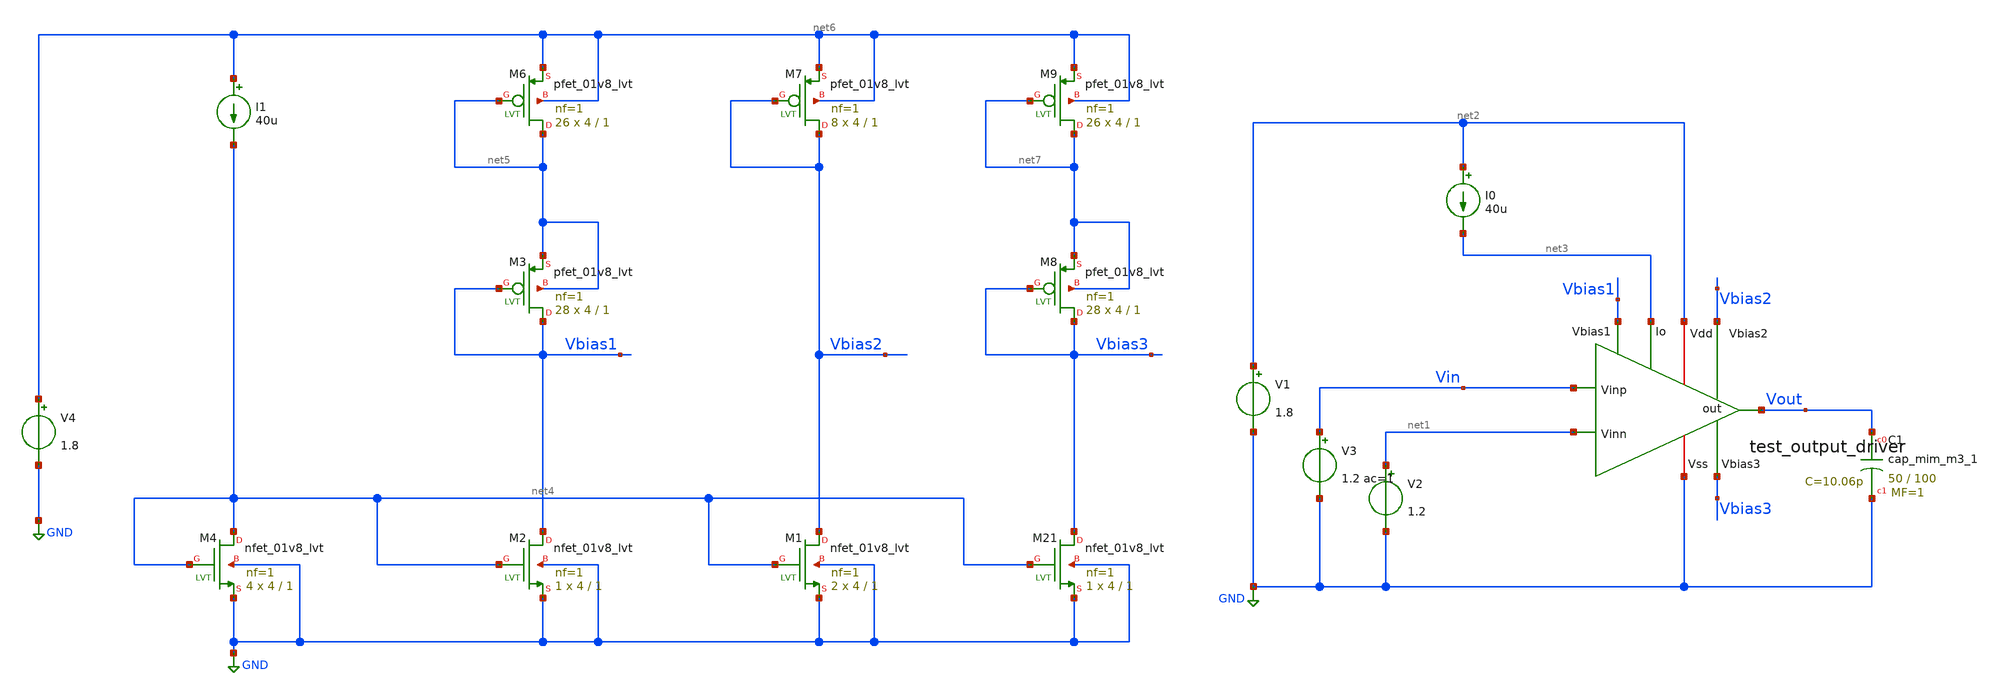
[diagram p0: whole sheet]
** sch_path: xschem/ip_block/opamp/folded_cas_xiaoyi/tb_test_output_driver.sch
**.subckt tb_test_output_driver
V1 net2 GND 1.8
V2 net1 GND 1.2
V3 Vin GND 1.2 ac=1
I0 net2 net3 40u
XC1 Vout GND sky130_fd_pr__cap_mim_m3_1 W=50 L=100 MF=1 m=1
x1 net2 net1 Vin Vout net3 GND Vbias1 Vbias2 Vbias3 test_output_driver
XM2 Vbias1 net4 GND GND sky130_fd_pr__nfet_01v8_lvt L=1 W=4 nf=1 ad='int((nf+1)/2) * W/nf * 0.29' as='int((nf+2)/2) * W/nf * 0.29'
+ pd='2*int((nf+1)/2) * (W/nf + 0.29)' ps='2*int((nf+2)/2) * (W/nf + 0.29)' nrd='0.29 / W' nrs='0.29 / W'
+ sa=0 sb=0 sd=0 mult=1 m=1
XM3 Vbias1 Vbias1 net5 net5 sky130_fd_pr__pfet_01v8_lvt L=1 W=4 nf=1 ad='int((nf+1)/2) * W/nf * 0.29'
+ as='int((nf+2)/2) * W/nf * 0.29' pd='2*int((nf+1)/2) * (W/nf + 0.29)' ps='2*int((nf+2)/2) * (W/nf + 0.29)'
+ nrd='0.29 / W' nrs='0.29 / W' sa=0 sb=0 sd=0 mult=28 m=28
I1 net6 net4 40u
XM4 net4 net4 GND GND sky130_fd_pr__nfet_01v8_lvt L=1 W=4 nf=1 ad='int((nf+1)/2) * W/nf * 0.29' as='int((nf+2)/2) * W/nf * 0.29'
+ pd='2*int((nf+1)/2) * (W/nf + 0.29)' ps='2*int((nf+2)/2) * (W/nf + 0.29)' nrd='0.29 / W' nrs='0.29 / W'
+ sa=0 sb=0 sd=0 mult=4 m=4
V4 net6 GND 1.8
XM1 Vbias2 net4 GND GND sky130_fd_pr__nfet_01v8_lvt L=1 W=4 nf=1 ad='int((nf+1)/2) * W/nf * 0.29' as='int((nf+2)/2) * W/nf * 0.29'
+ pd='2*int((nf+1)/2) * (W/nf + 0.29)' ps='2*int((nf+2)/2) * (W/nf + 0.29)' nrd='0.29 / W' nrs='0.29 / W'
+ sa=0 sb=0 sd=0 mult=2 m=2
XM21 Vbias3 net4 GND GND sky130_fd_pr__nfet_01v8_lvt L=1 W=4 nf=1 ad='int((nf+1)/2) * W/nf * 0.29' as='int((nf+2)/2) * W/nf * 0.29'
+ pd='2*int((nf+1)/2) * (W/nf + 0.29)' ps='2*int((nf+2)/2) * (W/nf + 0.29)' nrd='0.29 / W' nrs='0.29 / W'
+ sa=0 sb=0 sd=0 mult=1 m=1
XM6 net5 net5 net6 net6 sky130_fd_pr__pfet_01v8_lvt L=1 W=4 nf=1 ad='int((nf+1)/2) * W/nf * 0.29' as='int((nf+2)/2) * W/nf * 0.29'
+ pd='2*int((nf+1)/2) * (W/nf + 0.29)' ps='2*int((nf+2)/2) * (W/nf + 0.29)' nrd='0.29 / W' nrs='0.29 / W'
+ sa=0 sb=0 sd=0 mult=26 m=26
XM7 Vbias2 Vbias2 net6 net6 sky130_fd_pr__pfet_01v8_lvt L=1 W=4 nf=1 ad='int((nf+1)/2) * W/nf * 0.29'
+ as='int((nf+2)/2) * W/nf * 0.29' pd='2*int((nf+1)/2) * (W/nf + 0.29)' ps='2*int((nf+2)/2) * (W/nf + 0.29)'
+ nrd='0.29 / W' nrs='0.29 / W' sa=0 sb=0 sd=0 mult=8 m=8
XM8 Vbias3 Vbias3 net7 net7 sky130_fd_pr__pfet_01v8_lvt L=1 W=4 nf=1 ad='int((nf+1)/2) * W/nf * 0.29'
+ as='int((nf+2)/2) * W/nf * 0.29' pd='2*int((nf+1)/2) * (W/nf + 0.29)' ps='2*int((nf+2)/2) * (W/nf + 0.29)'
+ nrd='0.29 / W' nrs='0.29 / W' sa=0 sb=0 sd=0 mult=28 m=28
XM9 net7 net7 net6 net6 sky130_fd_pr__pfet_01v8_lvt L=1 W=4 nf=1 ad='int((nf+1)/2) * W/nf * 0.29' as='int((nf+2)/2) * W/nf * 0.29'
+ pd='2*int((nf+1)/2) * (W/nf + 0.29)' ps='2*int((nf+2)/2) * (W/nf + 0.29)' nrd='0.29 / W' nrs='0.29 / W'
+ sa=0 sb=0 sd=0 mult=26 m=26
**** begin user architecture code
.lib $::SKYWATER_MODELS/sky130.lib.spice tt


.option temp=27
.op
.ac dec 10 1 1G
*.tran 0.1n 100u

.control
ac dec 10 1 1G
*tran 0.1n 100u
*ac dec 10 1 1G
let phase = 180/PI*vp(Vout)

plot vdb(Vout) phase
*plot Vin_p Vout
.endc

.save all



**** end user architecture code
**.ends

* expanding   symbol:  ip_block/opamp/folded_cas_xiaoyi/test_output_driver.sym # of pins=9
** sym_path: xschem/ip_block/opamp/folded_cas_xiaoyi/test_output_driver.sym
** sch_path: xschem/ip_block/opamp/folded_cas_xiaoyi/test_output_driver.sch
.subckt test_output_driver Vdd Vinn Vinp Vout Io Vss Vbias1 Vbias2 Vbias3
*.ipin Io
*.ipin Vbias1
*.ipin Vinp
*.ipin Vinn
*.ipin Vbias2
*.ipin Vbias3
*.opin Vout
*.iopin Vdd
*.iopin Vss
XM1 net2 Vinp net1 Vss sky130_fd_pr__nfet_01v8_lvt L=1 W=8 nf=1 ad='int((nf+1)/2) * W/nf * 0.29' as='int((nf+2)/2) * W/nf * 0.29'
+ pd='2*int((nf+1)/2) * (W/nf + 0.29)' ps='2*int((nf+2)/2) * (W/nf + 0.29)' nrd='0.29 / W' nrs='0.29 / W'
+ sa=0 sb=0 sd=0 mult=40 m=40
XM2 net3 Vinn net1 Vss sky130_fd_pr__nfet_01v8_lvt L=1 W=8 nf=1 ad='int((nf+1)/2) * W/nf * 0.29' as='int((nf+2)/2) * W/nf * 0.29'
+ pd='2*int((nf+1)/2) * (W/nf + 0.29)' ps='2*int((nf+2)/2) * (W/nf + 0.29)' nrd='0.29 / W' nrs='0.29 / W'
+ sa=0 sb=0 sd=0 mult=40 m=40
XM3 net1 Vbias1 net4 Vss sky130_fd_pr__nfet_01v8_lvt L=1 W=8 nf=1 ad='int((nf+1)/2) * W/nf * 0.29' as='int((nf+2)/2) * W/nf * 0.29'
+ pd='2*int((nf+1)/2) * (W/nf + 0.29)' ps='2*int((nf+2)/2) * (W/nf + 0.29)' nrd='0.29 / W' nrs='0.29 / W'
+ sa=0 sb=0 sd=0 mult=16 m=16
XM4 net4 Io Vss Vss sky130_fd_pr__nfet_01v8_lvt L=1 W=8 nf=1 ad='int((nf+1)/2) * W/nf * 0.29' as='int((nf+2)/2) * W/nf * 0.29'
+ pd='2*int((nf+1)/2) * (W/nf + 0.29)' ps='2*int((nf+2)/2) * (W/nf + 0.29)' nrd='0.29 / W' nrs='0.29 / W'
+ sa=0 sb=0 sd=0 mult=16 m=16
XM10 Vout net6 net7 Vss sky130_fd_pr__nfet_01v8_lvt L=1 W=4 nf=1 ad='int((nf+1)/2) * W/nf * 0.29' as='int((nf+2)/2) * W/nf * 0.29'
+ pd='2*int((nf+1)/2) * (W/nf + 0.29)' ps='2*int((nf+2)/2) * (W/nf + 0.29)' nrd='0.29 / W' nrs='0.29 / W'
+ sa=0 sb=0 sd=0 mult=4 m=4
XM12 net7 net8 Vss Vss sky130_fd_pr__nfet_01v8_lvt L=1 W=4 nf=1 ad='int((nf+1)/2) * W/nf * 0.29' as='int((nf+2)/2) * W/nf * 0.29'
+ pd='2*int((nf+1)/2) * (W/nf + 0.29)' ps='2*int((nf+2)/2) * (W/nf + 0.29)' nrd='0.29 / W' nrs='0.29 / W'
+ sa=0 sb=0 sd=0 mult=4 m=4
XM15 Io Vbias1 net5 Vss sky130_fd_pr__nfet_01v8_lvt L=1 W=8 nf=1 ad='int((nf+1)/2) * W/nf * 0.29' as='int((nf+2)/2) * W/nf * 0.29'
+ pd='2*int((nf+1)/2) * (W/nf + 0.29)' ps='2*int((nf+2)/2) * (W/nf + 0.29)' nrd='0.29 / W' nrs='0.29 / W'
+ sa=0 sb=0 sd=0 mult=2 m=2
XM16 net5 Io Vss Vss sky130_fd_pr__nfet_01v8_lvt L=1 W=8 nf=1 ad='int((nf+1)/2) * W/nf * 0.29' as='int((nf+2)/2) * W/nf * 0.29'
+ pd='2*int((nf+1)/2) * (W/nf + 0.29)' ps='2*int((nf+2)/2) * (W/nf + 0.29)' nrd='0.29 / W' nrs='0.29 / W'
+ sa=0 sb=0 sd=0 mult=2 m=2
XM13 net3 Vbias2 Vdd Vdd sky130_fd_pr__pfet_01v8_lvt L=1 W=8 nf=1 ad='int((nf+1)/2) * W/nf * 0.29' as='int((nf+2)/2) * W/nf * 0.29'
+ pd='2*int((nf+1)/2) * (W/nf + 0.29)' ps='2*int((nf+2)/2) * (W/nf + 0.29)' nrd='0.29 / W' nrs='0.29 / W'
+ sa=0 sb=0 sd=0 mult=38 m=38
XM14 net2 Vbias2 Vdd Vdd sky130_fd_pr__pfet_01v8_lvt L=1 W=8 nf=1 ad='int((nf+1)/2) * W/nf * 0.29' as='int((nf+2)/2) * W/nf * 0.29'
+ pd='2*int((nf+1)/2) * (W/nf + 0.29)' ps='2*int((nf+2)/2) * (W/nf + 0.29)' nrd='0.29 / W' nrs='0.29 / W'
+ sa=0 sb=0 sd=0 mult=38 m=38
XM17 net6 Vbias3 net3 net3 sky130_fd_pr__pfet_01v8_lvt L=1 W=8 nf=1 ad='int((nf+1)/2) * W/nf * 0.29'
+ as='int((nf+2)/2) * W/nf * 0.29' pd='2*int((nf+1)/2) * (W/nf + 0.29)' ps='2*int((nf+2)/2) * (W/nf + 0.29)'
+ nrd='0.29 / W' nrs='0.29 / W' sa=0 sb=0 sd=0 mult=20 m=20
XM18 Vout Vbias3 net2 net2 sky130_fd_pr__pfet_01v8_lvt L=1 W=8 nf=1 ad='int((nf+1)/2) * W/nf * 0.29'
+ as='int((nf+2)/2) * W/nf * 0.29' pd='2*int((nf+1)/2) * (W/nf + 0.29)' ps='2*int((nf+2)/2) * (W/nf + 0.29)'
+ nrd='0.29 / W' nrs='0.29 / W' sa=0 sb=0 sd=0 mult=20 m=20
XM6 net6 net6 net8 Vss sky130_fd_pr__nfet_01v8_lvt L=1 W=4 nf=1 ad='int((nf+1)/2) * W/nf * 0.29' as='int((nf+2)/2) * W/nf * 0.29'
+ pd='2*int((nf+1)/2) * (W/nf + 0.29)' ps='2*int((nf+2)/2) * (W/nf + 0.29)' nrd='0.29 / W' nrs='0.29 / W'
+ sa=0 sb=0 sd=0 mult=4 m=4
XM7 net8 net8 Vss Vss sky130_fd_pr__nfet_01v8_lvt L=1 W=4 nf=1 ad='int((nf+1)/2) * W/nf * 0.29' as='int((nf+2)/2) * W/nf * 0.29'
+ pd='2*int((nf+1)/2) * (W/nf + 0.29)' ps='2*int((nf+2)/2) * (W/nf + 0.29)' nrd='0.29 / W' nrs='0.29 / W'
+ sa=0 sb=0 sd=0 mult=4 m=4
.ends

.GLOBAL GND
.end
